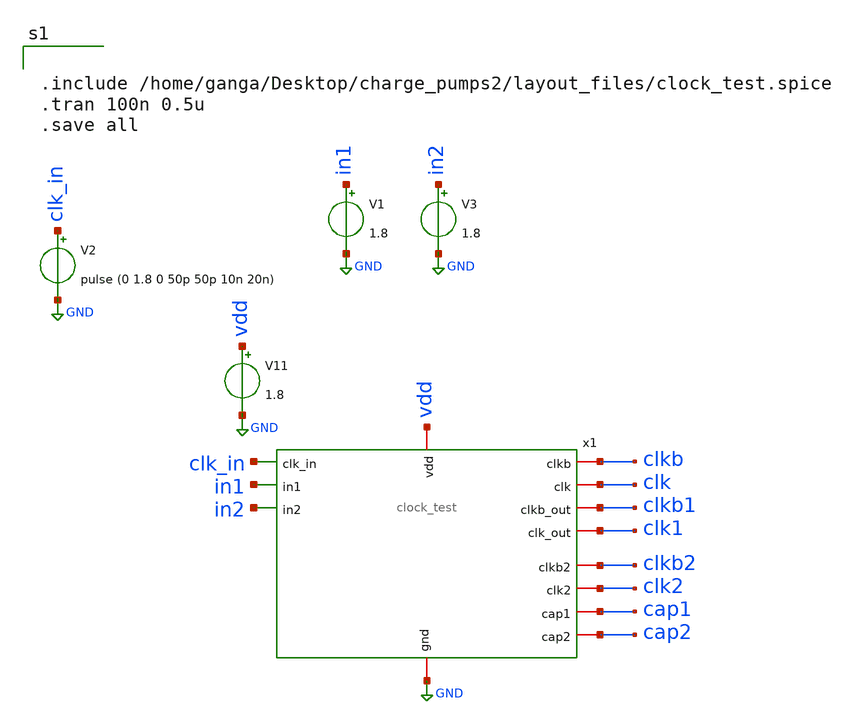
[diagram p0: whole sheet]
** sch_path: xschem/clock_tb.sch
**.subckt clock_tb
x1 clk_in vdd GND clk clkb in1 clkb1 clk1 in2 clk2 clkb2 cap1 cap2 clock_test
V2 clk_in GND pulse (0 1.8 0 50p 50p 10n 20n)
V11 vdd GND 1.8
V1 in1 GND 1.8
V3 in2 GND 1.8
**** begin user architecture code

** opencircuitdesign pdks install
.lib $::SKYWATER_MODELS/sky130.lib.spice tt




.include /home/ganga/Desktop/charge_pumps2/layout_files/clock_test.spice
.tran 100n 0.5u
.save all


**** end user architecture code
**.ends
.GLOBAL GND
.end
